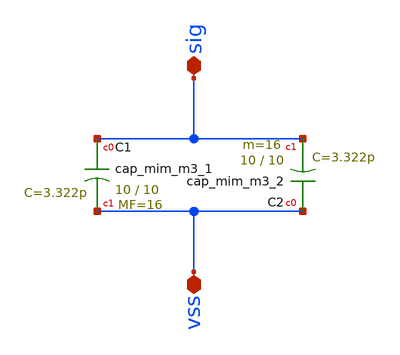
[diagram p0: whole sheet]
** sch_path: xschem/Switched_Caps/mim_cap_stacked_6pF.sch
**.subckt mim_cap_stacked_6pF sig vss
*.iopin sig
*.iopin vss
XC1 sig vss sky130_fd_pr__cap_mim_m3_1 W=10 L=10 MF=16 m=16
XC2 vss sig sky130_fd_pr__cap_mim_m3_2 W=10 L=10 MF=16 m=16
**.ends
.end
